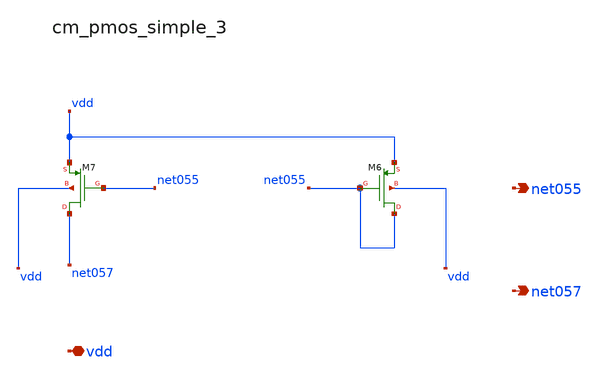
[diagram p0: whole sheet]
** sch_path: analog-db/raw/amp_013_qu2017_azc/hier/blocks/cm_pmos_simple_3.sch
**.subckt cm_pmos_simple_3 vdd net055 net057
*.iopin vdd
*.opin net055
*.opin net057
XM6 net055 net055 vdd vdd sg13_lv_pmos w=x_dut_xm6_w l=x_dut_xm6_l ng=1 m=x_dut_xm6_m
XM7 net057 net055 vdd vdd sg13_lv_pmos w=x_dut_xm7_w l=x_dut_xm7_l ng=1 m=x_dut_xm7_m
**.ends
.end
